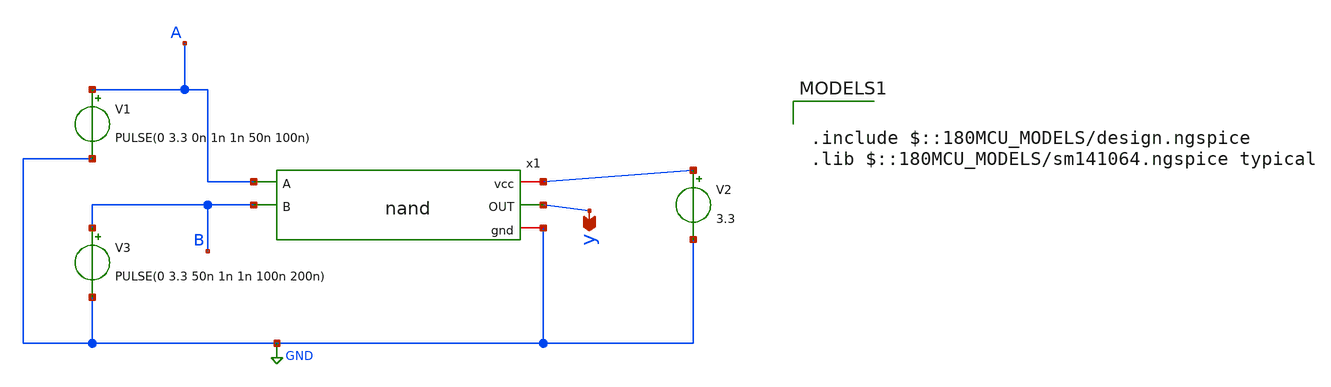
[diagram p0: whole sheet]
** sch_path: designs/schematics/mux2x1/nand_tb.sch
**.subckt nand_tb y
*.opin y
V1 A GND PULSE(0 3.3 0n 1n 1n 50n 100n)
V3 B GND PULSE(0 3.3 50n 1n 1n 100n 200n)
x1 net1 y A B GND nand
V2 net1 GND 3.3
**** begin user architecture code


.options method=trap rawfile=binary
.options solver=klu nomod
.control
save all

tran 1n 400n

write untitled-2.raw
.endc



.include $::180MCU_MODELS/design.ngspice
.lib $::180MCU_MODELS/sm141064.ngspice typical

**** end user architecture code
**.ends

* expanding   symbol:  voidwalkers-scandff-gf180mcu/designs/schematics/mux2x1/nand.sym # of pins=5
** sym_path: designs/schematics/mux2x1/nand.sym
** sch_path: designs/schematics/mux2x1/nand.sch
.subckt nand vcc OUT A B gnd
*.ipin A
*.ipin B
*.opin OUT
*.iopin vcc
*.iopin gnd
XM1 OUT B net1 gnd nfet_03v3 L=0.28u W=0.22u nf=1 ad='int((nf+1)/2) * W/nf * 0.18u' as='int((nf+2)/2) * W/nf * 0.18u'
+ pd='2*int((nf+1)/2) * (W/nf + 0.18u)' ps='2*int((nf+2)/2) * (W/nf + 0.18u)' nrd='0.18u / W' nrs='0.18u / W'
+ sa=0 sb=0 sd=0 m=1
XM2 net1 A gnd gnd nfet_03v3 L=0.28u W=0.22u nf=1 ad='int((nf+1)/2) * W/nf * 0.18u' as='int((nf+2)/2) * W/nf * 0.18u'
+ pd='2*int((nf+1)/2) * (W/nf + 0.18u)' ps='2*int((nf+2)/2) * (W/nf + 0.18u)' nrd='0.18u / W' nrs='0.18u / W'
+ sa=0 sb=0 sd=0 m=1
XM3 OUT A vcc vcc pfet_03v3 L=0.28u W=0.22u nf=1 ad='int((nf+1)/2) * W/nf * 0.18u' as='int((nf+2)/2) * W/nf * 0.18u'
+ pd='2*int((nf+1)/2) * (W/nf + 0.18u)' ps='2*int((nf+2)/2) * (W/nf + 0.18u)' nrd='0.18u / W' nrs='0.18u / W'
+ sa=0 sb=0 sd=0 m=1
XM4 OUT B vcc vcc pfet_03v3 L=0.28u W=0.22u nf=1 ad='int((nf+1)/2) * W/nf * 0.18u' as='int((nf+2)/2) * W/nf * 0.18u'
+ pd='2*int((nf+1)/2) * (W/nf + 0.18u)' ps='2*int((nf+2)/2) * (W/nf + 0.18u)' nrd='0.18u / W' nrs='0.18u / W'
+ sa=0 sb=0 sd=0 m=1
.ends

.GLOBAL GND
.end
